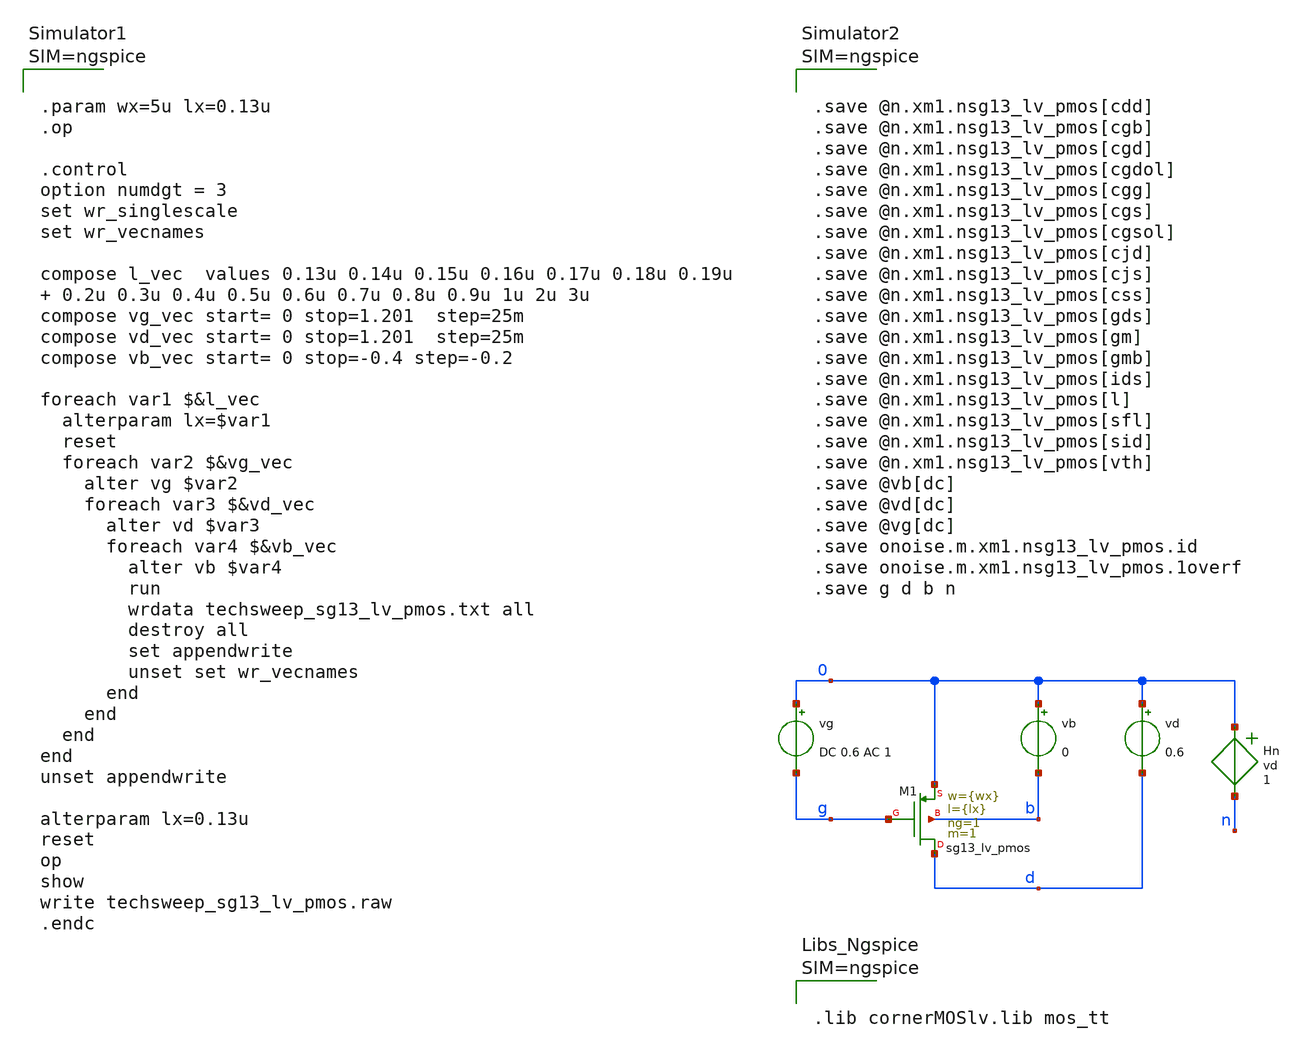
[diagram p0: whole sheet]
** sch_path: starter_files_open_source_tools/ihp-sg13cmos5l/techsweep_sg13_lv_pmos.sch
**.subckt techsweep_sg13_lv_pmos
Hn 0 n vd 1
vg 0 g DC 0.6 AC 1
vd 0 d 0.6
vb 0 b 0
XM1 d g 0 b sg13_lv_pmos w={wx} l={lx} ng=1 m=1 mm_ok=1
**** begin user architecture code



.save @n.xm1.nsg13_lv_pmos[cdd]
.save @n.xm1.nsg13_lv_pmos[cgb]
.save @n.xm1.nsg13_lv_pmos[cgd]
.save @n.xm1.nsg13_lv_pmos[cgdol]
.save @n.xm1.nsg13_lv_pmos[cgg]
.save @n.xm1.nsg13_lv_pmos[cgs]
.save @n.xm1.nsg13_lv_pmos[cgsol]
.save @n.xm1.nsg13_lv_pmos[cjd]
.save @n.xm1.nsg13_lv_pmos[cjs]
.save @n.xm1.nsg13_lv_pmos[css]
.save @n.xm1.nsg13_lv_pmos[gds]
.save @n.xm1.nsg13_lv_pmos[gm]
.save @n.xm1.nsg13_lv_pmos[gmb]
.save @n.xm1.nsg13_lv_pmos[ids]
.save @n.xm1.nsg13_lv_pmos[l]
.save @n.xm1.nsg13_lv_pmos[sfl]
.save @n.xm1.nsg13_lv_pmos[sid]
.save @n.xm1.nsg13_lv_pmos[vth]
.save @vb[dc]
.save @vd[dc]
.save @vg[dc]
.save onoise.m.xm1.nsg13_lv_pmos.id
.save onoise.m.xm1.nsg13_lv_pmos.1overf
.save g d b n






.param wx=5u lx=0.13u
.op

.control
option numdgt = 3
set wr_singlescale
set wr_vecnames

compose l_vec  values 0.13u 0.14u 0.15u 0.16u 0.17u 0.18u 0.19u  0.2u 0.3u 0.4u 0.5u 0.6u 0.7u 0.8u
+ 0.9u 1u 2u 3u
compose vg_vec start= 0 stop=1.201  step=25m
compose vd_vec start= 0 stop=1.201  step=25m
compose vb_vec start= 0 stop=-0.4 step=-0.2

foreach var1 $&l_vec
  alterparam lx=$var1
  reset
  foreach var2 $&vg_vec
    alter vg $var2
    foreach var3 $&vd_vec
      alter vd $var3
      foreach var4 $&vb_vec
        alter vb $var4
        run
        wrdata techsweep_sg13_lv_pmos.txt all
        destroy all
        set appendwrite
        unset set wr_vecnames
      end
    end
  end
end
unset appendwrite

alterparam lx=0.13u
reset
op
show
write techsweep_sg13_lv_pmos.raw
.endc






.lib cornerMOSlv.lib mos_tt



**** end user architecture code
**.ends
.end
